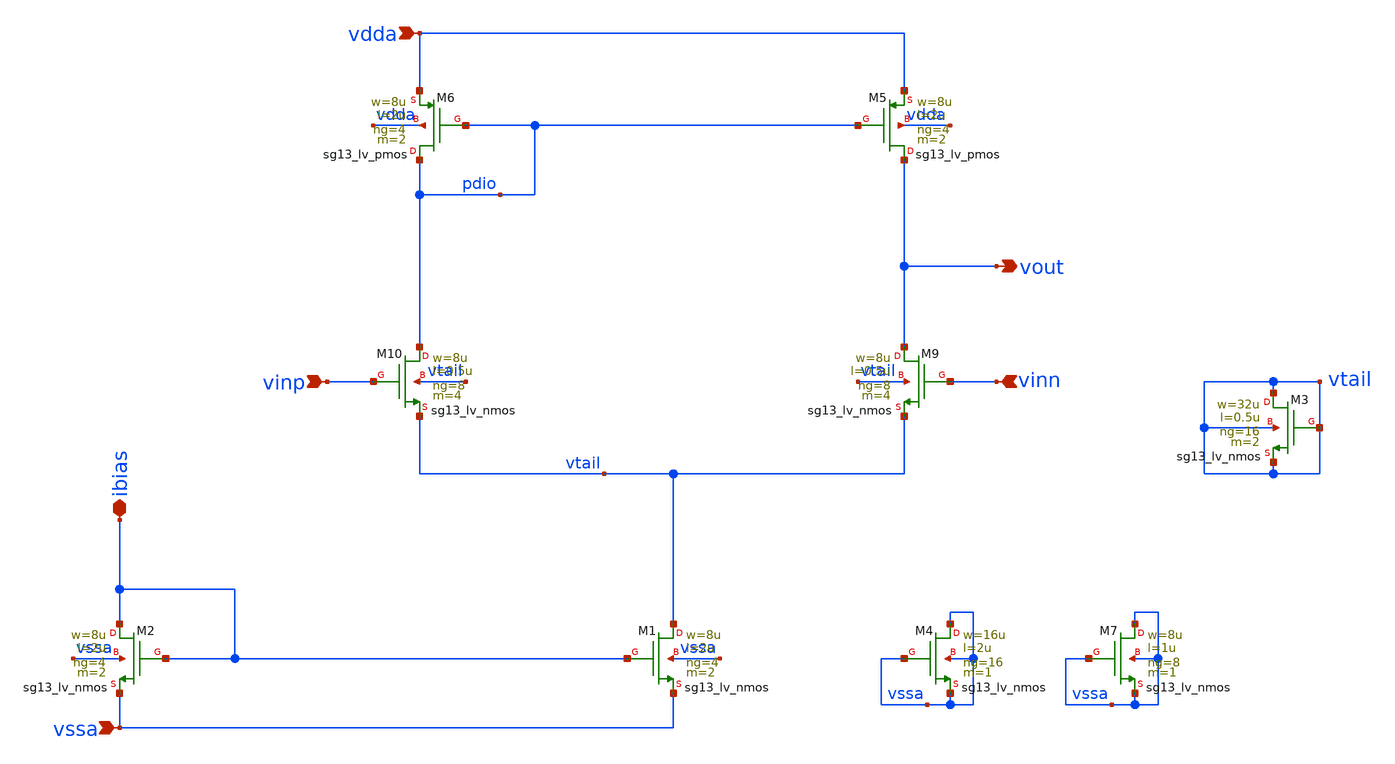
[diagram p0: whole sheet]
** sch_path: OTA_with_DNW/OTA.sch
**.subckt OTA ibias vdda vssa vinp vinn vout
*.iopin ibias
*.ipin vdda
*.ipin vssa
*.ipin vinp
*.ipin vinn
*.opin vout
XM5 vout pdio vdda vdda sg13_lv_pmos w=8u l=2u ng=4 m=2 mm_ok=1
XM6 pdio pdio vdda vdda sg13_lv_pmos w=8u l=2u ng=4 m=2 mm_ok=1
XM1 vtail ibias vssa vssa sg13_lv_nmos w=8u l=2u ng=4 m=2 mm_ok=1
XM2 ibias ibias vssa vssa sg13_lv_nmos w=8u l=2u ng=4 m=2 mm_ok=1
XM4 vssa vssa vssa vssa sg13_lv_nmos w=16u l=2u ng=16 m=1 mm_ok=1
XM7 vssa vssa vssa vssa sg13_lv_nmos w=8u l=1u ng=8 m=1 mm_ok=1
XM9 vout vinn vtail vtail sg13_lv_nmos w=8u l=0.5u ng=8 m=4 mm_ok=1
XM3 vtail vtail vtail vtail sg13_lv_nmos w=32u l=0.5u ng=16 m=2 mm_ok=1
XM10 pdio vinp vtail vtail sg13_lv_nmos w=8u l=0.5u ng=8 m=4 mm_ok=1
**.ends
.end
